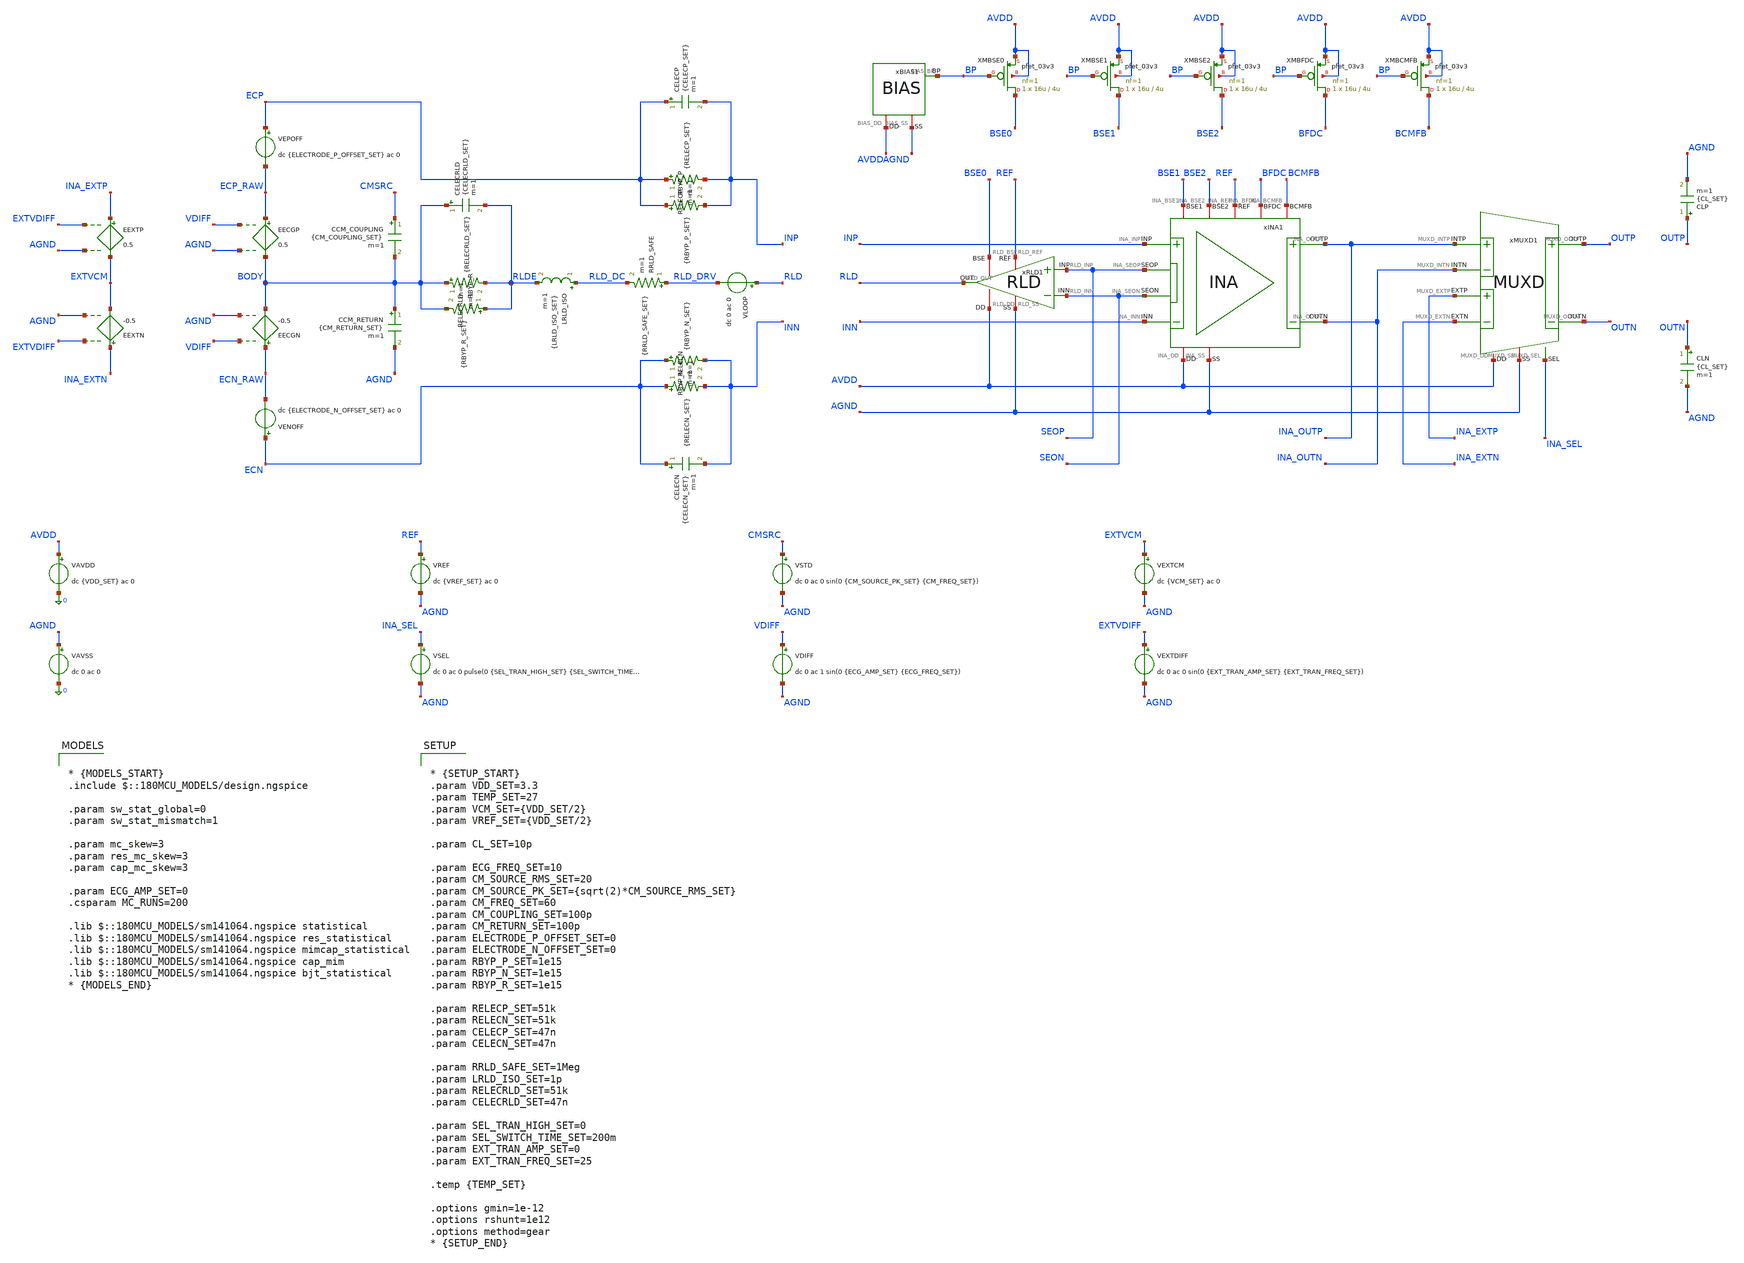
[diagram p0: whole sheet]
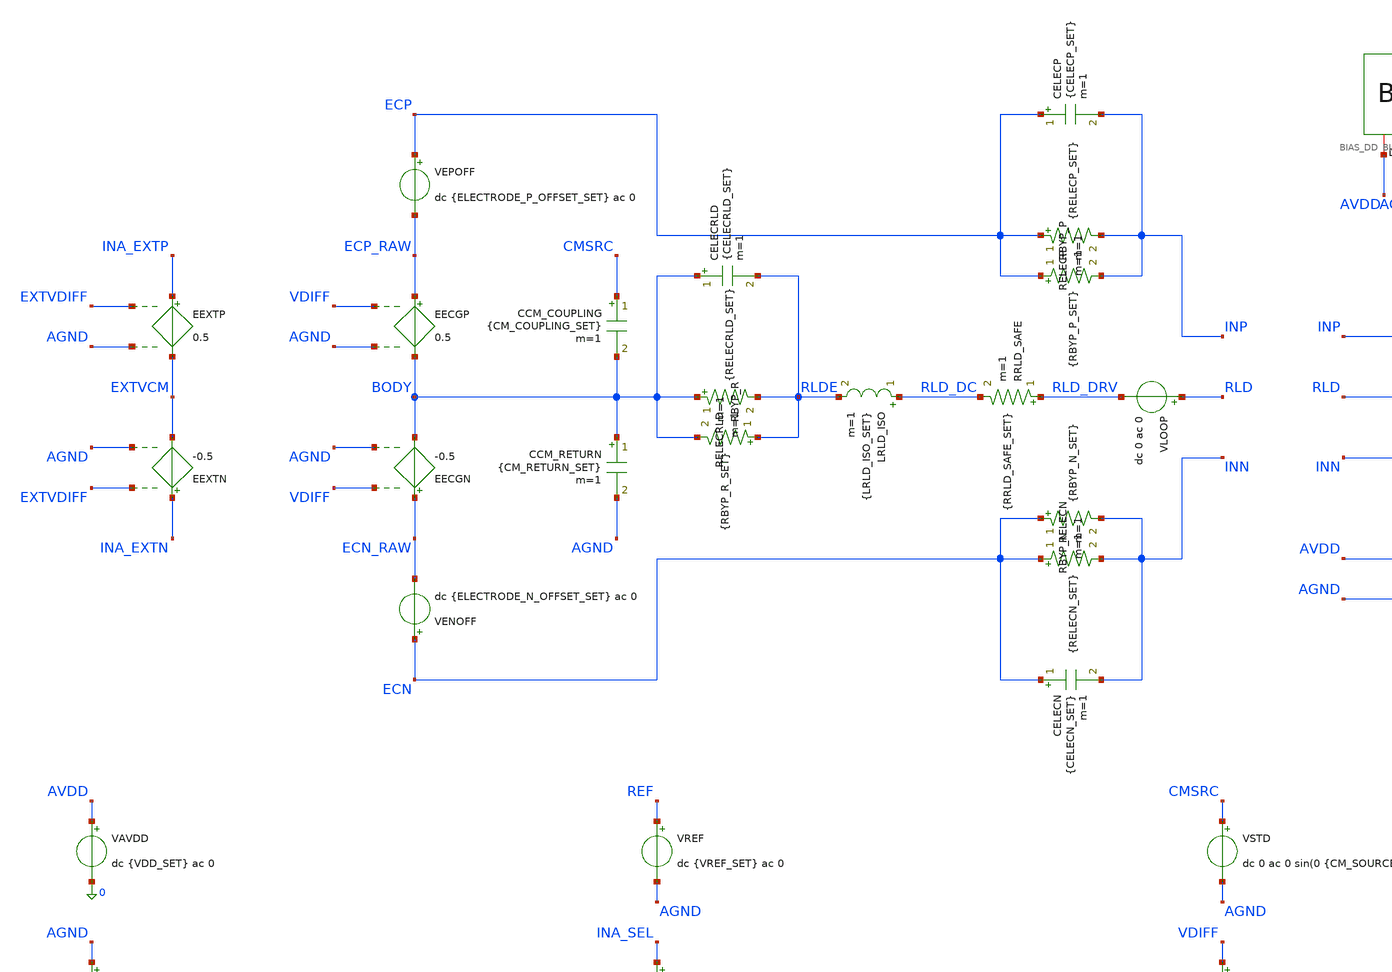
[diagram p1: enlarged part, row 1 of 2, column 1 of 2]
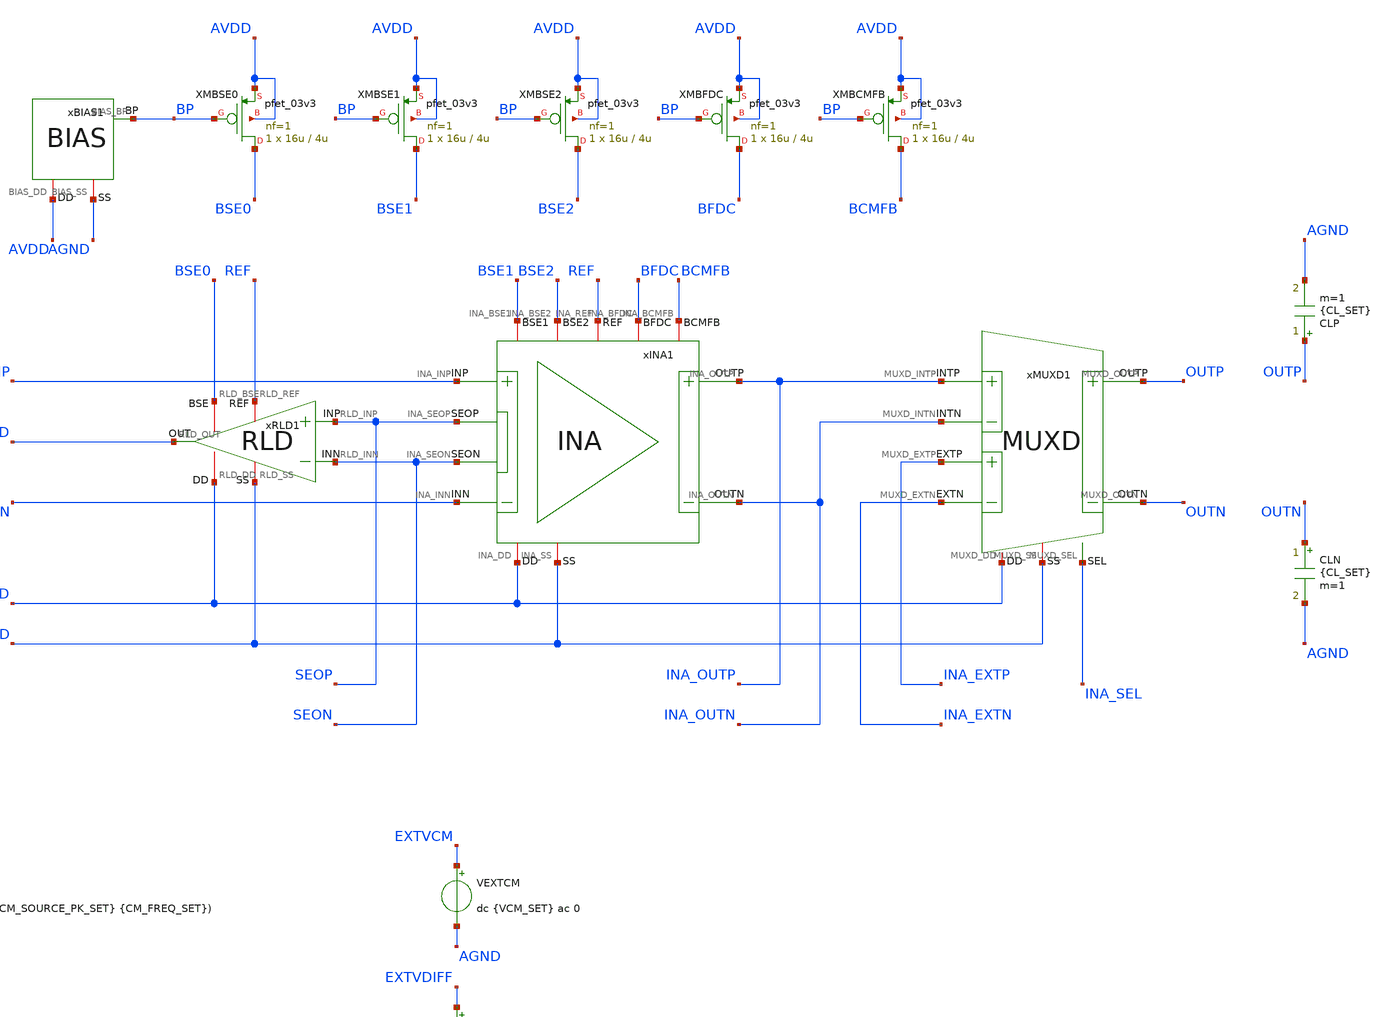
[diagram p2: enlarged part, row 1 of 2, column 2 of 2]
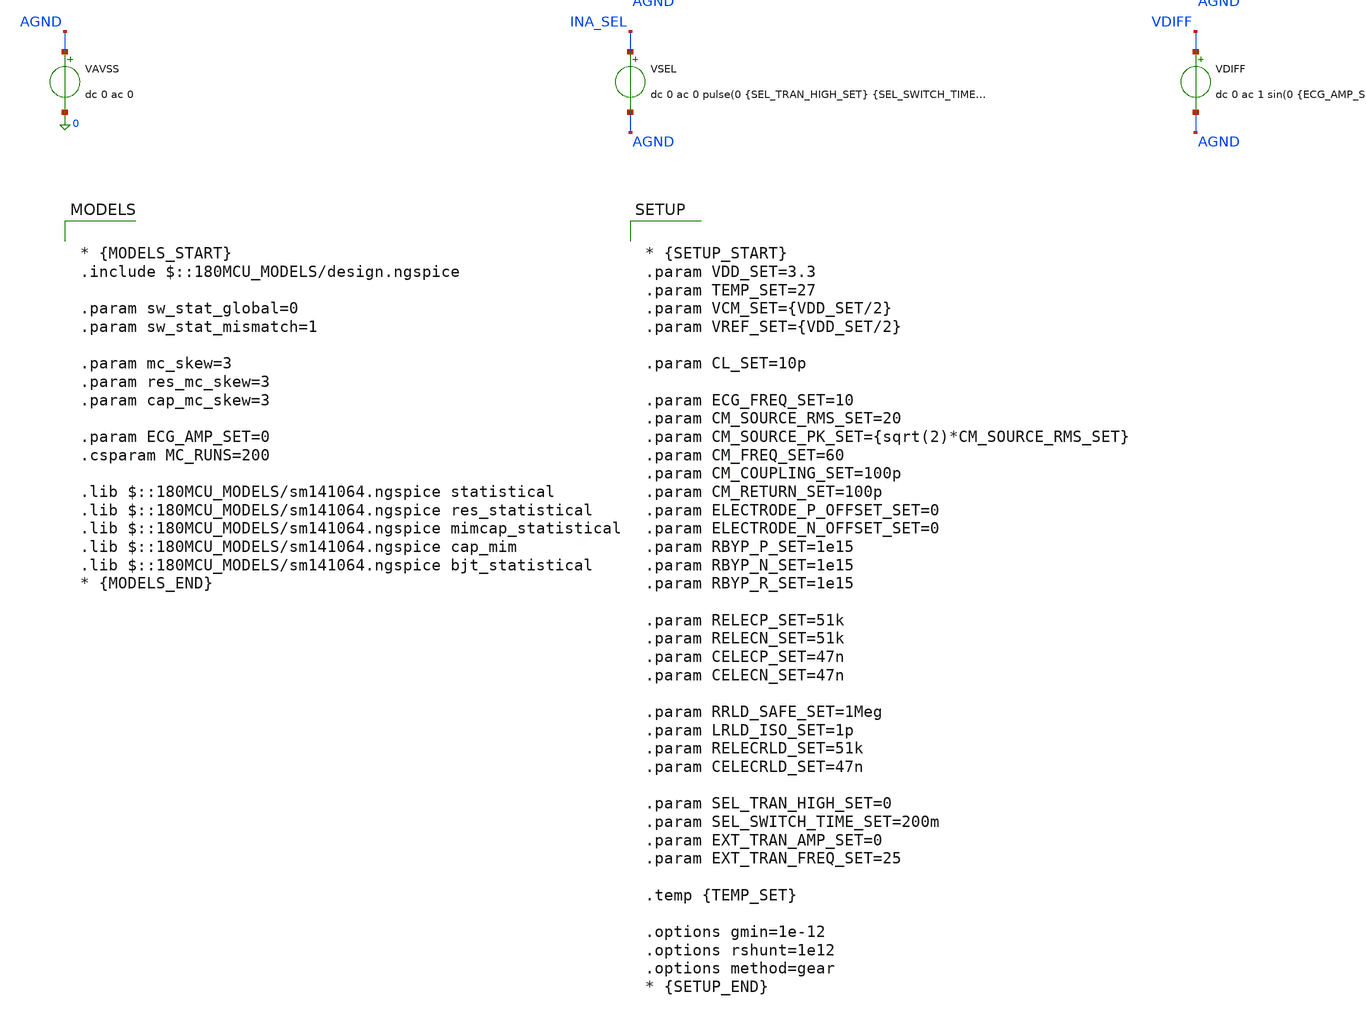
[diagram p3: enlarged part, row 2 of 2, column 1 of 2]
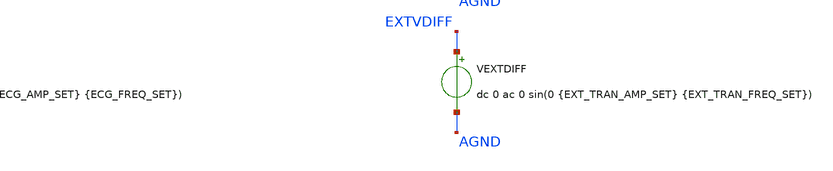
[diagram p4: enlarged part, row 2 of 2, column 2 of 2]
** sch_path: Design_Files/IC Design/Testbench/AFE_BLOCKS/INA_RLD/INA_RLD_TB_MC.sch
**.subckt INA_RLD_TB_MC
xMUXD1 AVDD AGND INA_OUTP INA_OUTN OUTN OUTP INA_EXTP INA_EXTN INA_SEL MUXD
xINA1 AVDD AGND INP INN INA_OUTN BFDC INA_OUTP BCMFB REF SEON SEOP BSE1 BSE2 INA
xRLD1 AVDD AGND SEOP SEON RLD REF BSE0 RLD
CLP OUTP AGND {CL_SET} m=1
CLN OUTN AGND {CL_SET} m=1
xBIAS1 AVDD AGND BP BIAS
XMBSE0 BSE0 BP AVDD AVDD pfet_03v3 L=4u W=16u nf=1 ad='int((nf+1)/2) * W/nf * 0.18u' as='int((nf+2)/2) * W/nf * 0.18u'
+ pd='2*int((nf+1)/2) * (W/nf + 0.18u)' ps='2*int((nf+2)/2) * (W/nf + 0.18u)' nrd='0.18u / W' nrs='0.18u / W'
+ sa=0 sb=0 sd=0 m=1
XMBSE1 BSE1 BP AVDD AVDD pfet_03v3 L=4u W=16u nf=1 ad='int((nf+1)/2) * W/nf * 0.18u' as='int((nf+2)/2) * W/nf * 0.18u'
+ pd='2*int((nf+1)/2) * (W/nf + 0.18u)' ps='2*int((nf+2)/2) * (W/nf + 0.18u)' nrd='0.18u / W' nrs='0.18u / W'
+ sa=0 sb=0 sd=0 m=1
XMBSE2 BSE2 BP AVDD AVDD pfet_03v3 L=4u W=16u nf=1 ad='int((nf+1)/2) * W/nf * 0.18u' as='int((nf+2)/2) * W/nf * 0.18u'
+ pd='2*int((nf+1)/2) * (W/nf + 0.18u)' ps='2*int((nf+2)/2) * (W/nf + 0.18u)' nrd='0.18u / W' nrs='0.18u / W'
+ sa=0 sb=0 sd=0 m=1
XMBFDC BFDC BP AVDD AVDD pfet_03v3 L=4u W=16u nf=1 ad='int((nf+1)/2) * W/nf * 0.18u' as='int((nf+2)/2) * W/nf * 0.18u'
+ pd='2*int((nf+1)/2) * (W/nf + 0.18u)' ps='2*int((nf+2)/2) * (W/nf + 0.18u)' nrd='0.18u / W' nrs='0.18u / W'
+ sa=0 sb=0 sd=0 m=1
XMBCMFB BCMFB BP AVDD AVDD pfet_03v3 L=4u W=16u nf=1 ad='int((nf+1)/2) * W/nf * 0.18u' as='int((nf+2)/2) * W/nf * 0.18u'
+ pd='2*int((nf+1)/2) * (W/nf + 0.18u)' ps='2*int((nf+2)/2) * (W/nf + 0.18u)' nrd='0.18u / W' nrs='0.18u / W'
+ sa=0 sb=0 sd=0 m=1
VAVDD AVDD 0 dc {VDD_SET} ac 0
.save i(vavdd)
VAVSS AGND 0 dc 0 ac 0
VSTD CMSRC AGND dc 0 ac 0 sin(0 {CM_SOURCE_PK_SET} {CM_FREQ_SET})
EECGP ECP_RAW BODY VDIFF AGND 0.5
EECGN ECN_RAW BODY VDIFF AGND -0.5
EEXTP INA_EXTP EXTVCM EXTVDIFF AGND 0.5
VDIFF VDIFF AGND dc 0 ac 1 sin(0 {ECG_AMP_SET} {ECG_FREQ_SET})
VLOOP RLD RLD_DRV dc 0 ac 0
.save i(vloop)
VSEL INA_SEL AGND dc 0 ac 0 pulse(0 {SEL_TRAN_HIGH_SET} {SEL_SWITCH_TIME_SET} 1u 1u 400m 800m)
VEXTCM EXTVCM AGND dc {VCM_SET} ac 0
VEXTDIFF EXTVDIFF AGND dc 0 ac 0 sin(0 {EXT_TRAN_AMP_SET} {EXT_TRAN_FREQ_SET})
EEXTN INA_EXTN EXTVCM EXTVDIFF AGND -0.5
CCM_COUPLING CMSRC BODY {CM_COUPLING_SET} m=1
RELECP ECP INP {RELECP_SET} m=1
RELECN ECN INN {RELECN_SET} m=1
CELECP ECP INP {CELECP_SET} m=1
CELECN ECN INN {CELECN_SET} m=1
RRLD_SAFE RLD_DRV RLD_DC {RRLD_SAFE_SET} m=1
RELECRLD BODY RLDE {RELECRLD_SET} m=1
CELECRLD BODY RLDE {CELECRLD_SET} m=1
VEPOFF ECP ECP_RAW dc {ELECTRODE_P_OFFSET_SET} ac 0
VENOFF ECN ECN_RAW dc {ELECTRODE_N_OFFSET_SET} ac 0
CCM_RETURN BODY AGND {CM_RETURN_SET} m=1
RBYP_P ECP INP {RBYP_P_SET} m=1
RBYP_N ECN INN {RBYP_N_SET} m=1
RBYP_R RLDE BODY {RBYP_R_SET} m=1
LRLD_ISO RLD_DC RLDE {LRLD_ISO_SET} m=1
VREF REF AGND dc {VREF_SET} ac 0
.save i(vref)
**** begin user architecture code

* {MODELS_START}
.include $::180MCU_MODELS/design.ngspice

.param sw_stat_global=0
.param sw_stat_mismatch=1

.param mc_skew=3
.param res_mc_skew=3
.param cap_mc_skew=3

.param ECG_AMP_SET=0
.csparam MC_RUNS=200

.lib $::180MCU_MODELS/sm141064.ngspice statistical
.lib $::180MCU_MODELS/sm141064.ngspice res_statistical
.lib $::180MCU_MODELS/sm141064.ngspice mimcap_statistical
.lib $::180MCU_MODELS/sm141064.ngspice cap_mim
.lib $::180MCU_MODELS/sm141064.ngspice bjt_statistical
* {MODELS_END}



* {SETUP_START}
.param VDD_SET=3.3
.param TEMP_SET=27
.param VCM_SET={VDD_SET/2}
.param VREF_SET={VDD_SET/2}

.param CL_SET=10p

.param ECG_FREQ_SET=10
.param CM_SOURCE_RMS_SET=20
.param CM_SOURCE_PK_SET={sqrt(2)*CM_SOURCE_RMS_SET}
.param CM_FREQ_SET=60
.param CM_COUPLING_SET=100p
.param CM_RETURN_SET=100p
.param ELECTRODE_P_OFFSET_SET=0
.param ELECTRODE_N_OFFSET_SET=0
.param RBYP_P_SET=1e15
.param RBYP_N_SET=1e15
.param RBYP_R_SET=1e15

.param RELECP_SET=51k
.param RELECN_SET=51k
.param CELECP_SET=47n
.param CELECN_SET=47n

.param RRLD_SAFE_SET=1Meg
.param LRLD_ISO_SET=1p
.param RELECRLD_SET=51k
.param CELECRLD_SET=47n

.param SEL_TRAN_HIGH_SET=0
.param SEL_SWITCH_TIME_SET=200m
.param EXT_TRAN_AMP_SET=0
.param EXT_TRAN_FREQ_SET=25

.temp {TEMP_SET}

.options gmin=1e-12
.options rshunt=1e12
.options method=gear
* {SETUP_END}




* {MEAS_START}
.control

destroy all

set noaskquit
set wr_singlescale
unset wr_vecnames

option klu
option numdgt=15
option method=gear
option maxord=2
option rshunt=1e12


let mode=0

dowhile mode < 3

* MODE

if mode = 0
set proc=MM
alterparam sw_stat_global=0
alterparam sw_stat_mismatch=1
end

if mode = 1
set proc=GL
alterparam sw_stat_global=1
alterparam sw_stat_mismatch=0
end

if mode = 2
set proc=FULL
alterparam sw_stat_global=1
alterparam sw_stat_mismatch=1
end

shell mkdir -p /foss/designs/ECG_Acquisition_IC/Measurement_Results/IC_Simulation/AFE_BLOCKS/INA_RLD/{$proc}.Result_txt

shell rm -f /foss/designs/ECG_Acquisition_IC/Measurement_Results/IC_Simulation/AFE_BLOCKS/INA_RLD/{$proc}.Result_txt/{$proc}.mc_summary.txt
shell rm -f /foss/designs/ECG_Acquisition_IC/Measurement_Results/IC_Simulation/AFE_BLOCKS/INA_RLD/{$proc}.Result_txt/{$proc}.mc_debug_op.txt

echo run idd_A power_W out_cm_error_V rld_dc_error_V vos_V s1_gain s2_gain ina_gain gain_error_pct rld_bw3db_Hz
+ rld_pm_deg cm_supp_60_dB cm_supp_150_dB ina_cmrr_60_dB ina_cmrr_150_dB rld_off_vin_cm_V > /foss/designs/ECG_Acquisition_IC/Measurement_Results/IC_Simulation/AFE_BLOCKS/INA_RLD/{$proc}.Result_txt/{$proc}.mc_summary.txt

echo run vos_V outp_V outn_V outcm_V outdiff_V ref_V rld_V body_V bp_V idd_A power_W > /foss/designs/ECG_Acquisition_IC/Measurement_Results/IC_Simulation/AFE_BLOCKS/INA_RLD/{$proc}.Result_txt/{$proc}.mc_debug_op.txt

let run=1
let mc_runs=$&MC_RUNS

dowhile run <= mc_runs

set runnum=$&run

setseed $runnum
mc_source


option klu
option numdgt=15
option method=gear
option maxord=2
option rshunt=1e12


* SOURCES

alter @VAVDD[DC]=3.3
alter @VAVSS[DC]=0

alter @VSTD[DC]=0
alter @VEPOFF[DC]=0
alter @VENOFF[DC]=0

alter @VDIFF[DC]=0
alter @VLOOP[DC]=0

alter @VSEL[DC]=0

alter @VEXTCM[DC]=1.65
alter @VEXTDIFF[DC]=0

alter @VREF[DC]=1.65

alter @VAVDD[ACMAG]=0
alter @VAVSS[ACMAG]=0
alter @VSTD[ACMAG]=0
alter @VEPOFF[ACMAG]=0
alter @VENOFF[ACMAG]=0
alter @VDIFF[ACMAG]=0
alter @VLOOP[ACMAG]=0
alter @VEXTCM[ACMAG]=0
alter @VEXTDIFF[ACMAG]=0
alter @VREF[ACMAG]=0


* NOMINAL ELECTRODE MODEL

alter RELECP 51k
alter RELECN 51k
alter CELECP 47n
alter CELECN 47n
alter RELECRLD 51k
alter CELECRLD 47n
alter RBYP_P 1e15
alter RBYP_N 1e15
alter RBYP_R 1e15

alter RRLD_SAFE 1Meg
alter LRLD_ISO 1p


save AVDD AGND BP REF
save INP INN SEOP SEON
save INA_OUTP INA_OUTN
save OUTP OUTN
save RLD RLD_DRV BODY CMSRC
save VDIFF

save vavdd#branch
save vloop#branch

save @m.xmbse0.m0[id]
save @m.xmbse1.m0[id]
save @m.xmbse2.m0[id]
save @m.xmbfdc.m0[id]
save @m.xmbcmfb.m0[id]


* OFFSET

alter @VDIFF[DC]=0

dc VDIFF -3m 3m 300u

let outdiff_sweep=v(INA_OUTP)-v(INA_OUTN)

meas dc vos_meas when outdiff_sweep=0 cross=1

set vos_val=$&vos_meas

destroy all


* CENTER OP

alter @VDIFF[DC]=$vos_val

alter @VDIFF[ACMAG]=0
alter @VSTD[ACMAG]=0
alter @VLOOP[ACMAG]=0
alter @VAVDD[ACMAG]=0
alter @VAVSS[ACMAG]=0
alter @VREF[ACMAG]=0

alter RRLD_SAFE 1Meg

op

let outp=v(OUTP)-v(AGND)
let outn=v(OUTN)-v(AGND)

let outcm=0.5*(outp+outn)
let outdiff=outp-outn

let ref=v(REF)-v(AGND)

let rld=v(RLD)-v(AGND)
let body=v(BODY)-v(AGND)
let bp=v(BP)-v(AGND)

let out_cm_error=outcm-ref
let rld_dc_error=rld-ref

let idd_total=abs(vavdd#branch)
let power_total=(v(AVDD)-v(AGND))*idd_total

set outp_val=$&outp
set outn_val=$&outn
set outcm_val=$&outcm
set outdiff_val=$&outdiff

set ref_val=$&ref
set rld_val=$&rld
set body_val=$&body
set bp_val=$&bp

set out_cm_error_val=$&out_cm_error
set rld_dc_error_val=$&rld_dc_error

set idd_val=$&idd_total
set power_val=$&power_total


echo $runnum $vos_val $outp_val $outn_val $outcm_val $outdiff_val $ref_val $rld_val $body_val $bp_val
+ $idd_val $power_val >> /foss/designs/ECG_Acquisition_IC/Measurement_Results/IC_Simulation/AFE_BLOCKS/INA_RLD/{$proc}.Result_txt/{$proc}.mc_debug_op.txt

destroy all


* INA AC

alter RRLD_SAFE 1Meg

alter @VDIFF[DC]=$vos_val

alter @VDIFF[ACMAG]=1
alter @VDIFF[ACPHASE]=0

alter @VSTD[ACMAG]=0
alter @VLOOP[ACMAG]=0
alter @VEXTDIFF[ACMAG]=0
alter @VAVDD[ACMAG]=0
alter @VAVSS[ACMAG]=0
alter @VREF[ACMAG]=0

ac lin 15 10 150

let vin_diff=v(INP)-v(INN)
let se_diff=v(SEOP)-v(SEON)
let ina_out_diff=v(INA_OUTP)-v(INA_OUTN)

let s1_gain=mag(se_diff/vin_diff)
let s2_gain=mag(ina_out_diff/se_diff)
let ina_gain=mag(ina_out_diff/vin_diff)

let s1_gain_10_meas=s1_gain[0]
let s2_gain_10_meas=s2_gain[0]
let ina_gain_10_meas=ina_gain[0]

let ina_gain_60_meas=ina_gain[5]
let ina_gain_150_meas=ina_gain[14]

let gain_error_pct=100*(ina_gain_10_meas/240-1)

set s1_gain_val=$&s1_gain_10_meas
set s2_gain_val=$&s2_gain_10_meas
set ina_gain_val=$&ina_gain_10_meas

set ina_gain_60_val=$&ina_gain_60_meas
set ina_gain_150_val=$&ina_gain_150_meas

set gain_error_val=$&gain_error_pct

destroy all


* RLD OFF + INA CMRR

* Keep the DC bias; isolate the RLD path in AC.
alter RRLD_SAFE 1Meg
alter LRLD_ISO 1e12

alter @VDIFF[ACMAG]=0

alter @VSTD[ACMAG]=1
alter @VSTD[ACPHASE]=0

alter @VLOOP[ACMAG]=0
alter @VEXTDIFF[ACMAG]=0
alter @VAVDD[ACMAG]=0
alter @VAVSS[ACMAG]=0
alter @VREF[ACMAG]=0

op

let rld_off_vin_cm=0.5*(v(INP)+v(INN))-v(AGND)
set rld_off_vin_cm_val=$&rld_off_vin_cm

destroy all

ac lin 3 60 150

let vin_cm=0.5*(v(INP)+v(INN))-v(AGND)
let ina_out_diff=v(INA_OUTP)-v(INA_OUTN)

let vin_cm_mag=mag(vin_cm)
let ina_acm=mag(ina_out_diff/vin_cm)

* [0] = 60 Hz; [2] = 150 Hz
let vin_cm_off_60_meas=vin_cm_mag[0]
let vin_cm_off_150_meas=vin_cm_mag[2]

let ina_acm_60_meas=ina_acm[0]
let ina_acm_150_meas=ina_acm[2]

set vin_cm_off_60_val=$&vin_cm_off_60_meas
set vin_cm_off_150_val=$&vin_cm_off_150_meas

set ina_acm_60_val=$&ina_acm_60_meas
set ina_acm_150_val=$&ina_acm_150_meas

let ina_cmrr_60=20*log10($ina_gain_60_val/$ina_acm_60_val)
let ina_cmrr_150=20*log10($ina_gain_150_val/$ina_acm_150_val)

set ina_cmrr_60_val=$&ina_cmrr_60
set ina_cmrr_150_val=$&ina_cmrr_150

destroy all


* RLD ON

alter RRLD_SAFE 1Meg
alter LRLD_ISO 1p

alter @VDIFF[ACMAG]=0

alter @VSTD[ACMAG]=1
alter @VSTD[ACPHASE]=0

alter @VLOOP[ACMAG]=0
alter @VEXTDIFF[ACMAG]=0
alter @VAVDD[ACMAG]=0
alter @VAVSS[ACMAG]=0
alter @VREF[ACMAG]=0

ac lin 3 60 150

let vin_cm=0.5*(v(INP)+v(INN))-v(AGND)
let vin_cm_mag=mag(vin_cm)

* [0] = 60 Hz; [2] = 150 Hz
let vin_cm_on_60_meas=vin_cm_mag[0]
let vin_cm_on_150_meas=vin_cm_mag[2]

set vin_cm_on_60_val=$&vin_cm_on_60_meas
set vin_cm_on_150_val=$&vin_cm_on_150_meas

let cm_supp_60=20*log10($vin_cm_off_60_val/$vin_cm_on_60_val)
let cm_supp_150=20*log10($vin_cm_off_150_val/$vin_cm_on_150_val)

set cm_supp_60_val=$&cm_supp_60
set cm_supp_150_val=$&cm_supp_150

destroy all


* RLD LOOP

alter RRLD_SAFE 1Meg
alter LRLD_ISO 1p

alter @VDIFF[ACMAG]=0
alter @VSTD[ACMAG]=0

alter @VLOOP[ACMAG]=1
alter @VLOOP[ACPHASE]=0

alter @VEXTDIFF[ACMAG]=0
alter @VAVDD[ACMAG]=0
alter @VAVSS[ACMAG]=0
alter @VREF[ACMAG]=0

ac dec 20 0.01 10k

let loop_in=v(RLD_DRV)-v(AGND)
let loop_out=v(RLD)-v(AGND)

let loop_tf=-loop_out/loop_in

let loop_gain=mag(loop_tf)
let loop_phase=(180/3.141592653589793)*cph(loop_tf)

meas ac rld_lf_gain_meas find loop_gain at=0.01
let rld_bw_target=rld_lf_gain_meas/sqrt(2)
meas ac rld_bw3db_meas when loop_gain=$&rld_bw_target fall=1

meas ac rld_ugf_meas when loop_gain=1 fall=1

meas ac rld_phase_ugf_meas find loop_phase at=$&rld_ugf_meas

let rld_pm=180+rld_phase_ugf_meas

set rld_bw3db_val=$&rld_bw3db_meas
set rld_pm_val=$&rld_pm

destroy all


* SUMMARY

echo $runnum $idd_val $power_val $out_cm_error_val $rld_dc_error_val $vos_val $s1_gain_val $s2_gain_val
+ $ina_gain_val $gain_error_val $rld_bw3db_val $rld_pm_val $cm_supp_60_val $cm_supp_150_val $ina_cmrr_60_val
+ $ina_cmrr_150_val $rld_off_vin_cm_val >> /foss/designs/ECG_Acquisition_IC/Measurement_Results/IC_Simulation/AFE_BLOCKS/INA_RLD/{$proc}.Result_txt/{$proc}.mc_summary.txt


let run=run+1

end

let mode=mode+1

end


quit

.endc
* {MEAS_END}


**** end user architecture code
**.ends
.end
